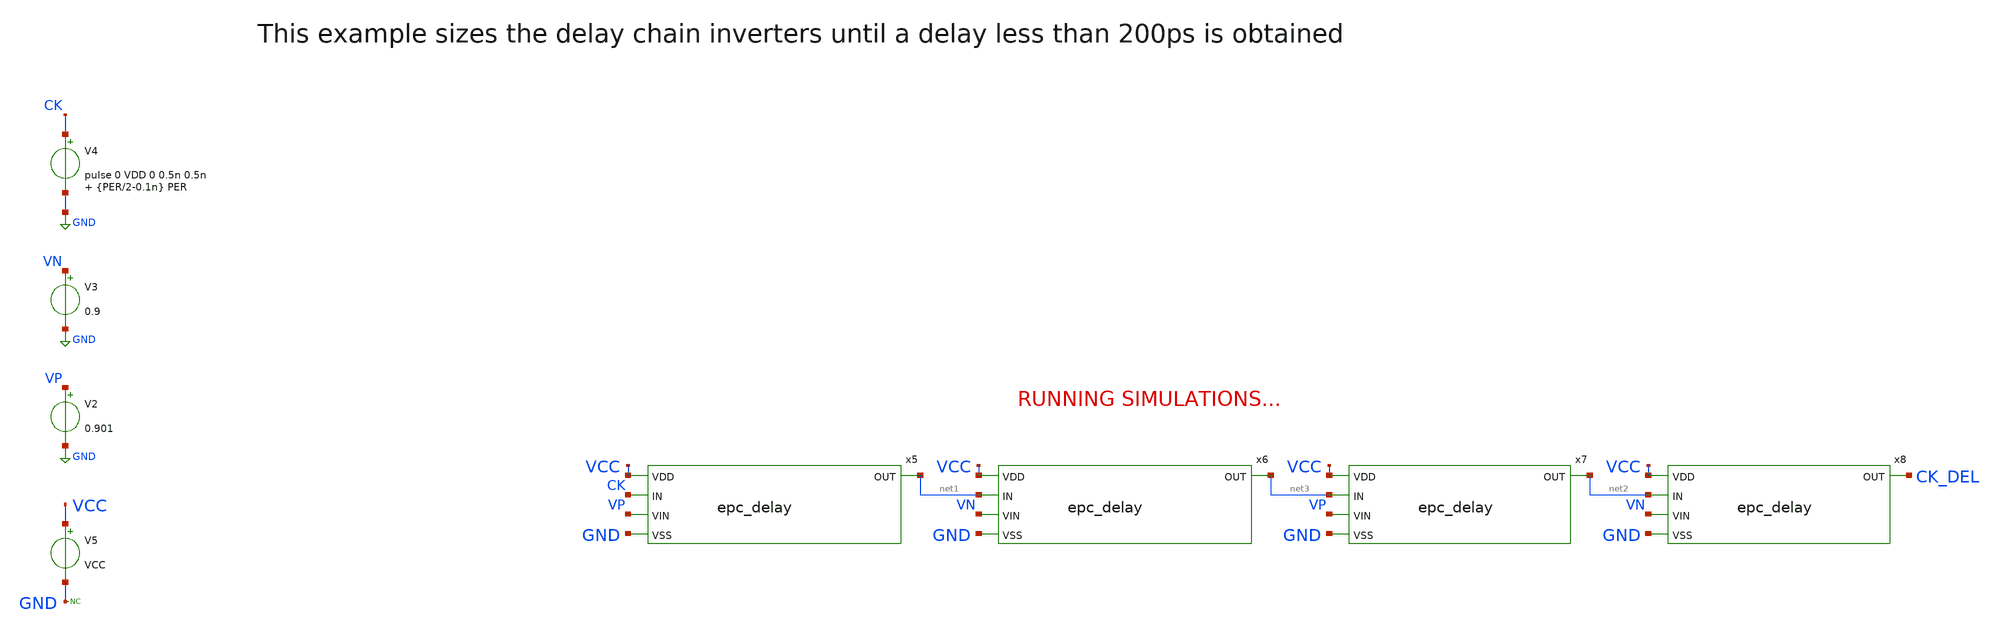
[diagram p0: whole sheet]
** sch_path: xschem/epc_delay_optimize.sch
.lib $::SKYWATER_MODELS/sky130.lib.spice tt
.include $::SKYWATER_STDCELLS/sky130_fd_sc_hd.spice

**.subckt epc_delay_optimize
V2 VP GND 0.901
V3 VN GND 0.9
V4 CK GND pulse 0 VDD 0 0.5n 0.5n {PER/2-0.1n} PER
V5 VCC GND VCC
* noconn GND
x5 VCC CK net1 VP GND epc_delay
x6 VCC net1 net3 VN GND epc_delay
x7 VCC net3 net2 VP GND epc_delay
x8 VCC net2 CK_DEL VN GND epc_delay
**** begin user architecture code


.param VCC=1.8
.param FREQ=0.5e6
.param PER={1/FREQ}
.param ILOAD=100u
.control
  save all
  set nobreak
  set numdgt=3
  set wr_singlescale
  set wr_vecnames
  tran 4p 2u
  write optimize_delay.raw
  * wrdata result.txt ck ck_del
  meas tran del
  + TRIG v(CK) TD=15n VAL=0.9 RISE=1
  + TARG v(CK_DEL) TD=15n VAL=0.9 RISE=1
  print del > result.txt
  quit 0
.endc


**** end user architecture code
**.ends
.GLOBAL GND
.end
